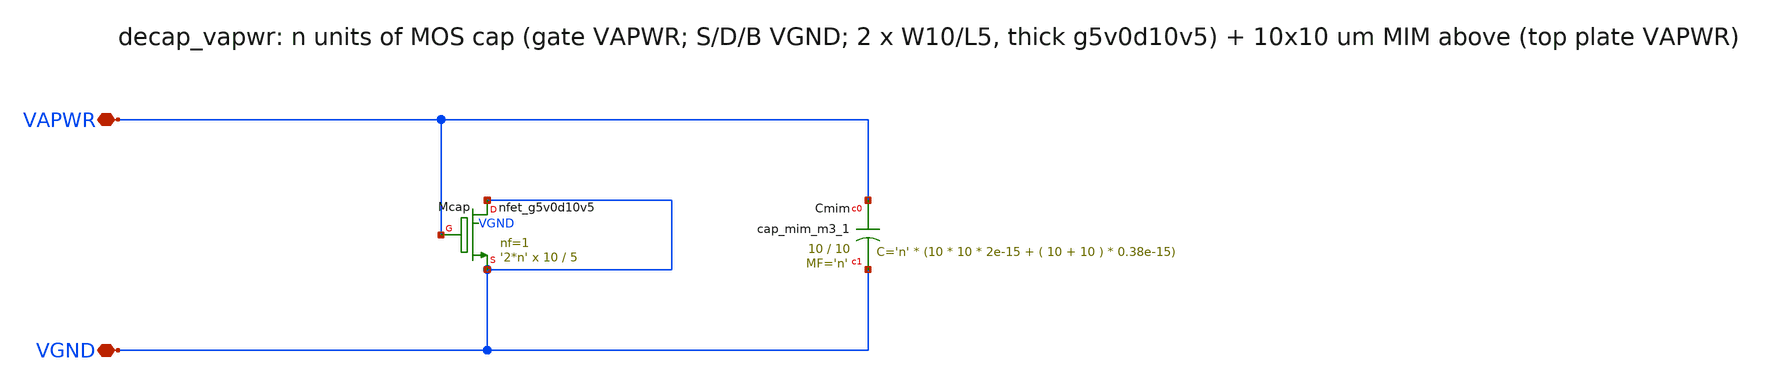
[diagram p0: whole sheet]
** sch_path: xschem/decap_vapwr.sch
**.subckt decap_vapwr VAPWR VGND
*.iopin VAPWR
*.iopin VGND
XMcap VGND VAPWR VGND VGND sky130_fd_pr__nfet_g5v0d10v5 L=5 W=10 nf=1 ad='int((nf+1)/2) * W/nf * 0.29'
+ as='int((nf+2)/2) * W/nf * 0.29' pd='2*int((nf+1)/2) * (W/nf + 0.29)' ps='2*int((nf+2)/2) * (W/nf + 0.29)'
+ nrd='0.29 / W' nrs='0.29 / W' sa=0 sb=0 sd=0 mult='2*n' m='2*n'
XCmim VAPWR VGND sky130_fd_pr__cap_mim_m3_1 W=10 L=10 MF='n' m='n'
**.ends
.end
